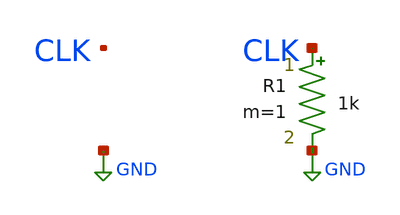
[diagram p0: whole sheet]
** sch_path: sim/jitter-calibration/testbench/tb_jitter_calibration.sch
**.subckt tb_jitter_calibration
R1 CLK GND 1k m=1
**** begin user architecture code

** GENERATED -- variant J10c: 300 cycles, nominal period
** 3.9170 ns, injected period jitter 1.000000% RMS
** (seeded RNG, seed 185010), TR = TF = 1 ns.
VCLK CLK GND pwl(  0.000000n 0 1.500000n 0 2.500000n 1.8 3.467587n 1.8  4.467587n 0 5.435174n 0
+ 6.435174n 1.8 7.412706n 1.8  8.412706n 0 9.390239n 0 10.390239n 1.8 11.309488n 1.8  12.309488n 0 13.228738n 0
+ 14.228738n 1.8 15.200628n 1.8  16.200628n 0 17.172519n 0 18.172519n 1.8 19.153921n 1.8  20.153921n 0
+ 21.135324n 0 22.135324n 1.8 23.078011n 1.8  24.078011n 0 25.020698n 0 26.020698n 1.8 26.951104n 1.8
+  27.951104n 0 28.881509n 0 29.881509n 1.8 30.850456n 1.8  31.850456n 0 32.819404n 0 33.819404n 1.8 34.771235n
+ 1.8  35.771235n 0 36.723066n 0 37.723066n 1.8 38.689098n 1.8  39.689098n 0 40.655130n 0 41.655130n 1.8
+ 42.608410n 1.8  43.608410n 0 44.561691n 0 45.561691n 1.8 46.506346n 1.8  47.506346n 0 48.451000n 0 49.451000n
+ 1.8 50.422296n 1.8  51.422296n 0 52.393592n 0 53.393592n 1.8 54.347858n 1.8  55.347858n 0 56.302123n 0
+ 57.302123n 1.8 58.256420n 1.8  59.256420n 0 60.210717n 0 61.210717n 1.8 62.173219n 1.8  63.173219n 0
+ 64.135720n 0 65.135720n 1.8 66.089666n 1.8  67.089666n 0 68.043611n 0 69.043611n 1.8 70.009970n 1.8
+  71.009970n 0 71.976329n 0 72.976329n 1.8 73.930021n 1.8  74.930021n 0 75.883714n 0 76.883714n 1.8 77.869536n
+ 1.8  78.869536n 0 79.855357n 0 80.855357n 1.8 81.766974n 1.8  82.766974n 0 83.678592n 0 84.678592n 1.8
+ 85.653946n 1.8  86.653946n 0 87.629300n 0 88.629300n 1.8 89.565099n 1.8  90.565099n 0 91.500898n 0 92.500898n
+ 1.8 93.444309n 1.8  94.444309n 0 95.387720n 0 96.387720n 1.8 97.308553n 1.8  98.308553n 0 99.229386n 0
+ 100.229386n 1.8 101.204522n 1.8  102.204522n 0 103.179659n 0 104.179659n 1.8 105.107584n 1.8  106.107584n 0
+ 107.035510n 0 108.035510n 1.8 108.976588n 1.8  109.976588n 0 110.917665n 0 111.917665n 1.8 112.867539n 1.8
+  113.867539n 0 114.817412n 0 115.817412n 1.8 116.788125n 1.8  117.788125n 0 118.758838n 0 119.758838n 1.8
+ 120.705444n 1.8  121.705444n 0 122.652051n 0 123.652051n 1.8 124.610528n 1.8  125.610528n 0 126.569005n 0
+ 127.569005n 1.8 128.502948n 1.8  129.502948n 0 130.436891n 0 131.436891n 1.8 132.374925n 1.8  133.374925n 0
+ 134.312958n 0 135.312958n 1.8 136.284613n 1.8  137.284613n 0 138.256268n 0 139.256268n 1.8 140.186354n 1.8
+  141.186354n 0 142.116440n 0 143.116440n 1.8 144.083552n 1.8  145.083552n 0 146.050664n 0 147.050664n 1.8
+ 148.011420n 1.8  149.011420n 0 149.972176n 0 150.972176n 1.8 151.931191n 1.8  152.931191n 0 153.890206n 0
+ 154.890206n 1.8 155.821172n 1.8  156.821172n 0 157.752138n 0 158.752138n 1.8 159.703538n 1.8  160.703538n 0
+ 161.654938n 0 162.654938n 1.8 163.603802n 1.8  164.603802n 0 165.552666n 0 166.552666n 1.8 167.494949n 1.8
+  168.494949n 0 169.437233n 0 170.437233n 1.8 171.428640n 1.8  172.428640n 0 173.420048n 0 174.420048n 1.8
+ 175.354551n 1.8  176.354551n 0 177.289054n 0 178.289054n 1.8 179.229152n 1.8  180.229152n 0 181.169250n 0
+ 182.169250n 1.8 183.108568n 1.8  184.108568n 0 185.047886n 0 186.047886n 1.8 186.977655n 1.8  187.977655n 0
+ 188.907423n 0 189.907423n 1.8 190.855155n 1.8  191.855155n 0 192.802888n 0 193.802888n 1.8 194.758147n 1.8
+  195.758147n 0 196.713406n 0 197.713406n 1.8 198.647563n 1.8  199.647563n 0 200.581720n 0 201.581720n 1.8
+ 202.490503n 1.8  203.490503n 0 204.399286n 0 205.399286n 1.8 206.354163n 1.8  207.354163n 0 208.309039n 0
+ 209.309039n 1.8 210.263509n 1.8  211.263509n 0 212.217979n 0 213.217979n 1.8 214.190097n 1.8  215.190097n 0
+ 216.162214n 0 217.162214n 1.8 218.112178n 1.8  219.112178n 0 220.062141n 0 221.062141n 1.8 222.028435n 1.8
+  223.028435n 0 223.994728n 0 224.994728n 1.8 225.974648n 1.8  226.974648n 0 227.954567n 0 228.954567n 1.8
+ 229.901638n 1.8  230.901638n 0 231.848708n 0 232.848708n 1.8 233.815738n 1.8  234.815738n 0 235.782768n 0
+ 236.782768n 1.8 237.752998n 1.8  238.752998n 0 239.723229n 0 240.723229n 1.8 241.679197n 1.8  242.679197n 0
+ 243.635165n 0 244.635165n 1.8 245.579002n 1.8  246.579002n 0 247.522838n 0 248.522838n 1.8 249.470750n 1.8
+  250.470750n 0 251.418663n 0 252.418663n 1.8 253.424114n 1.8  254.424114n 0 255.429565n 0 256.429565n 1.8
+ 257.421423n 1.8  258.421423n 0 259.413281n 0 260.413281n 1.8 261.371691n 1.8  262.371691n 0 263.330100n 0
+ 264.330100n 1.8 265.331600n 1.8  266.331600n 0 267.333100n 0 268.333100n 1.8 269.275644n 1.8  270.275644n 0
+ 271.218188n 0 272.218188n 1.8 273.182219n 1.8  274.182219n 0 275.146251n 0 276.146251n 1.8 277.122987n 1.8
+  278.122987n 0 279.099724n 0 280.099724n 1.8 281.059622n 1.8  282.059622n 0 283.019520n 0 284.019520n 1.8
+ 284.976046n 1.8  285.976046n 0 286.932571n 0 287.932571n 1.8 288.866826n 1.8  289.866826n 0 290.801080n 0
+ 291.801080n 1.8 292.718970n 1.8  293.718970n 0 294.636859n 0 295.636859n 1.8 296.602262n 1.8  297.602262n 0
+ 298.567664n 0 299.567664n 1.8 300.514107n 1.8  301.514107n 0 302.460550n 0 303.460550n 1.8 304.452856n 1.8
+  305.452856n 0 306.445163n 0 307.445163n 1.8 308.358824n 1.8  309.358824n 0 310.272485n 0 311.272485n 1.8
+ 312.204532n 1.8  313.204532n 0 314.136578n 0 315.136578n 1.8 316.094694n 1.8  317.094694n 0 318.052810n 0
+ 319.052810n 1.8 320.001457n 1.8  321.001457n 0 321.950104n 0 322.950104n 1.8 323.893454n 1.8  324.893454n 0
+ 325.836804n 0 326.836804n 1.8 327.820440n 1.8  328.820440n 0 329.804075n 0 330.804075n 1.8 331.750001n 1.8
+  332.750001n 0 333.695927n 0 334.695927n 1.8 335.657631n 1.8  336.657631n 0 337.619335n 0 338.619335n 1.8
+ 339.604657n 1.8  340.604657n 0 341.589979n 0 342.589979n 1.8 343.534561n 1.8  344.534561n 0 345.479143n 0
+ 346.479143n 1.8 347.428678n 1.8  348.428678n 0 349.378213n 0 350.378213n 1.8 351.316855n 1.8  352.316855n 0
+ 353.255497n 0 354.255497n 1.8 355.209135n 1.8  356.209135n 0 357.162773n 0 358.162773n 1.8 359.154792n 1.8
+  360.154792n 0 361.146811n 0 362.146811n 1.8 363.099707n 1.8  364.099707n 0 365.052604n 0 366.052604n 1.8
+ 367.000733n 1.8  368.000733n 0 368.948863n 0 369.948863n 1.8 370.905355n 1.8  371.905355n 0 372.861847n 0
+ 373.861847n 1.8 374.854057n 1.8  375.854057n 0 376.846266n 0 377.846266n 1.8 378.783298n 1.8  379.783298n 0
+ 380.720331n 0 381.720331n 1.8 382.691373n 1.8  383.691373n 0 384.662415n 0 385.662415n 1.8 386.617329n 1.8
+  387.617329n 0 388.572244n 0 389.572244n 1.8 390.541558n 1.8  391.541558n 0 392.510873n 0 393.510873n 1.8
+ 394.455352n 1.8  395.455352n 0 396.399832n 0 397.399832n 1.8 398.379878n 1.8  399.379878n 0 400.359924n 0
+ 401.359924n 1.8 402.346665n 1.8  403.346665n 0 404.333407n 0 405.333407n 1.8 406.269845n 1.8  407.269845n 0
+ 408.206282n 0 409.206282n 1.8 410.179704n 1.8  411.179704n 0 412.153125n 0 413.153125n 1.8 414.072846n 1.8
+  415.072846n 0 415.992567n 0 416.992567n 1.8 417.953025n 1.8  418.953025n 0 419.913483n 0 420.913483n 1.8
+ 421.859298n 1.8  422.859298n 0 423.805114n 0 424.805114n 1.8 425.734864n 1.8  426.734864n 0 427.664615n 0
+ 428.664615n 1.8 429.634682n 1.8  430.634682n 0 431.604749n 0 432.604749n 1.8 433.567902n 1.8  434.567902n 0
+ 435.531054n 0 436.531054n 1.8 437.506541n 1.8  438.506541n 0 439.482028n 0 440.482028n 1.8 441.430071n 1.8
+  442.430071n 0 443.378114n 0 444.378114n 1.8 445.341175n 1.8  446.341175n 0 447.304236n 0 448.304236n 1.8
+ 449.254138n 1.8  450.254138n 0 451.204040n 0 452.204040n 1.8 453.183686n 1.8  454.183686n 0 455.163332n 0
+ 456.163332n 1.8 457.105453n 1.8  458.105453n 0 459.047574n 0 460.047574n 1.8 460.997655n 1.8  461.997655n 0
+ 462.947736n 0 463.947736n 1.8 464.909671n 1.8  465.909671n 0 466.871606n 0 467.871606n 1.8 468.820058n 1.8
+  469.820058n 0 470.768510n 0 471.768510n 1.8 472.716913n 1.8  473.716913n 0 474.665317n 0 475.665317n 1.8
+ 476.629255n 1.8  477.629255n 0 478.593193n 0 479.593193n 1.8 480.569885n 1.8  481.569885n 0 482.546576n 0
+ 483.546576n 1.8 484.509378n 1.8  485.509378n 0 486.472179n 0 487.472179n 1.8 488.435751n 1.8  489.435751n 0
+ 490.399322n 0 491.399322n 1.8 492.356471n 1.8  493.356471n 0 494.313621n 0 495.313621n 1.8 496.311841n 1.8
+  497.311841n 0 498.310062n 0 499.310062n 1.8 500.281417n 1.8  501.281417n 0 502.252772n 0 503.252772n 1.8
+ 504.223085n 1.8  505.223085n 0 506.193398n 0 507.193398n 1.8 508.172969n 1.8  509.172969n 0 510.152540n 0
+ 511.152540n 1.8 512.150574n 1.8  513.150574n 0 514.148607n 0 515.148607n 1.8 516.108316n 1.8  517.108316n 0
+ 518.068024n 0 519.068024n 1.8 520.021929n 1.8  521.021929n 0 521.975834n 0 522.975834n 1.8 523.956108n 1.8
+  524.956108n 0 525.936381n 0 526.936381n 1.8 527.903064n 1.8  528.903064n 0 529.869747n 0 530.869747n 1.8
+ 531.853980n 1.8  532.853980n 0 533.838214n 0 534.838214n 1.8 535.816551n 1.8  536.816551n 0 537.794889n 0
+ 538.794889n 1.8 539.727189n 1.8  540.727189n 0 541.659489n 0 542.659489n 1.8 543.641375n 1.8  544.641375n 0
+ 545.623261n 0 546.623261n 1.8 547.605233n 1.8  548.605233n 0 549.587204n 0 550.587204n 1.8 551.560022n 1.8
+  552.560022n 0 553.532839n 0 554.532839n 1.8 555.485706n 1.8  556.485706n 0 557.438573n 0 558.438573n 1.8
+ 559.410459n 1.8  560.410459n 0 561.382345n 0 562.382345n 1.8 563.355811n 1.8  564.355811n 0 565.329276n 0
+ 566.329276n 1.8 567.285830n 1.8  568.285830n 0 569.242384n 0 570.242384n 1.8 571.212968n 1.8  572.212968n 0
+ 573.183552n 0 574.183552n 1.8 575.168164n 1.8  576.168164n 0 577.152777n 0 578.152777n 1.8 579.150439n 1.8
+  580.150439n 0 581.148101n 0 582.148101n 1.8 583.071739n 1.8  584.071739n 0 584.995377n 0 585.995377n 1.8
+ 586.939910n 1.8  587.939910n 0 588.884444n 0 589.884444n 1.8 590.831208n 1.8  591.831208n 0 592.777972n 0
+ 593.777972n 1.8 594.738809n 1.8  595.738809n 0 596.699645n 0 597.699645n 1.8 598.654166n 1.8  599.654166n 0
+ 600.608686n 0 601.608686n 1.8 602.593648n 1.8  603.593648n 0 604.578610n 0 605.578610n 1.8 606.545995n 1.8
+  607.545995n 0 608.513380n 0 609.513380n 1.8 610.456717n 1.8  611.456717n 0 612.400053n 0 613.400053n 1.8
+ 614.369379n 1.8  615.369379n 0 616.338706n 0 617.338706n 1.8 618.322239n 1.8  619.322239n 0 620.305773n 0
+ 621.305773n 1.8 622.258676n 1.8  623.258676n 0 624.211580n 0 625.211580n 1.8 626.163616n 1.8  627.163616n 0
+ 628.115652n 0 629.115652n 1.8 630.110946n 1.8  631.110946n 0 632.106239n 0 633.106239n 1.8 634.094996n 1.8
+  635.094996n 0 636.083753n 0 637.083753n 1.8 638.022007n 1.8  639.022007n 0 639.960262n 0 640.960262n 1.8
+ 641.944529n 1.8  642.944529n 0 643.928795n 0 644.928795n 1.8 645.874505n 1.8  646.874505n 0 647.820216n 0
+ 648.820216n 1.8 649.801482n 1.8  650.801482n 0 651.782748n 0 652.782748n 1.8 653.747596n 1.8  654.747596n 0
+ 655.712444n 0 656.712444n 1.8 657.678982n 1.8  658.678982n 0 659.645520n 0 660.645520n 1.8 661.591855n 1.8
+  662.591855n 0 663.538191n 0 664.538191n 1.8 665.485187n 1.8  666.485187n 0 667.432183n 0 668.432183n 1.8
+ 669.419227n 1.8  670.419227n 0 671.406271n 0 672.406271n 1.8 673.327805n 1.8  674.327805n 0 675.249339n 0
+ 676.249339n 1.8 677.232033n 1.8  678.232033n 0 679.214728n 0 680.214728n 1.8 681.164308n 1.8  682.164308n 0
+ 683.113889n 0 684.113889n 1.8 685.070725n 1.8  686.070725n 0 687.027561n 0 688.027561n 1.8 688.951112n 1.8
+  689.951112n 0 690.874662n 0 691.874662n 1.8 692.824420n 1.8  693.824420n 0 694.774178n 0 695.774178n 1.8
+ 696.726560n 1.8  697.726560n 0 698.678943n 0 699.678943n 1.8 700.652020n 1.8  701.652020n 0 702.625096n 0
+ 703.625096n 1.8 704.580270n 1.8  705.580270n 0 706.535444n 0 707.535444n 1.8 708.505501n 1.8  709.505501n 0
+ 710.475557n 0 711.475557n 1.8 712.421978n 1.8  713.421978n 0 714.368399n 0 715.368399n 1.8 716.348113n 1.8
+  717.348113n 0 718.327828n 0 719.327828n 1.8 720.286338n 1.8  721.286338n 0 722.244848n 0 723.244848n 1.8
+ 724.212968n 1.8  725.212968n 0 726.181087n 0 727.181087n 1.8 728.160394n 1.8  729.160394n 0 730.139702n 0
+ 731.139702n 1.8 732.088990n 1.8  733.088990n 0 734.038277n 0 735.038277n 1.8 735.991439n 1.8  736.991439n 0
+ 737.944601n 0 738.944601n 1.8 739.904355n 1.8  740.904355n 0 741.864108n 0 742.864108n 1.8 743.838251n 1.8
+  744.838251n 0 745.812393n 0 746.812393n 1.8 747.749591n 1.8  748.749591n 0 749.686789n 0 750.686789n 1.8
+ 751.650370n 1.8  752.650370n 0 753.613950n 0 754.613950n 1.8 755.573553n 1.8  756.573553n 0 757.533156n 0
+ 758.533156n 1.8 759.486980n 1.8  760.486980n 0 761.440804n 0 762.440804n 1.8 763.414867n 1.8  764.414867n 0
+ 765.388930n 0 766.388930n 1.8 767.379078n 1.8  768.379078n 0 769.369225n 0 770.369225n 1.8 771.333516n 1.8
+  772.333516n 0 773.297807n 0 774.297807n 1.8 775.209412n 1.8  776.209412n 0 777.121017n 0 778.121017n 1.8
+ 779.089050n 1.8  780.089050n 0 781.057084n 0 782.057084n 1.8 783.036384n 1.8  784.036384n 0 785.015684n 0
+ 786.015684n 1.8 787.000672n 1.8  788.000672n 0 788.985660n 0 789.985660n 1.8 790.919575n 1.8  791.919575n 0
+ 792.853490n 0 793.853490n 1.8 794.821912n 1.8  795.821912n 0 796.790334n 0 797.790334n 1.8 798.738880n 1.8
+  799.738880n 0 800.687425n 0 801.687425n 1.8 802.663109n 1.8  803.663109n 0 804.638793n 0 805.638793n 1.8
+ 806.576830n 1.8  807.576830n 0 808.514868n 0 809.514868n 1.8 810.476025n 1.8  811.476025n 0 812.437183n 0
+ 813.437183n 1.8 814.387642n 1.8  815.387642n 0 816.338101n 0 817.338101n 1.8 818.257021n 1.8  819.257021n 0
+ 820.175940n 0 821.175940n 1.8 822.089536n 1.8  823.089536n 0 824.003131n 0 825.003131n 1.8 825.950594n 1.8
+  826.950594n 0 827.898057n 0 828.898057n 1.8 829.878284n 1.8  830.878284n 0 831.858510n 0 832.858510n 1.8
+ 833.817286n 1.8  834.817286n 0 835.776062n 0 836.776062n 1.8 837.753702n 1.8  838.753702n 0 839.731342n 0
+ 840.731342n 1.8 841.673754n 1.8  842.673754n 0 843.616167n 0 844.616167n 1.8 845.558898n 1.8  846.558898n 0
+ 847.501629n 0 848.501629n 1.8 849.460750n 1.8  850.460750n 0 851.419870n 0 852.419870n 1.8 853.366837n 1.8
+  854.366837n 0 855.313804n 0 856.313804n 1.8 857.300954n 1.8  858.300954n 0 859.288103n 0 860.288103n 1.8
+ 861.269714n 1.8  862.269714n 0 863.251325n 0 864.251325n 1.8 865.231208n 1.8  866.231208n 0 867.211090n 0
+ 868.211090n 1.8 869.145106n 1.8  870.145106n 0 871.079121n 0 872.079121n 1.8 873.066848n 1.8  874.066848n 0
+ 875.054574n 0 876.054574n 1.8 877.001563n 1.8  878.001563n 0 878.948552n 0 879.948552n 1.8 880.922436n 1.8
+  881.922436n 0 882.896320n 0 883.896320n 1.8 884.858595n 1.8  885.858595n 0 886.820870n 0 887.820870n 1.8
+ 888.795133n 1.8  889.795133n 0 890.769397n 0 891.769397n 1.8 892.728198n 1.8  893.728198n 0 894.686998n 0
+ 895.686998n 1.8 896.647773n 1.8  897.647773n 0 898.608547n 0 899.608547n 1.8 900.580286n 1.8  901.580286n 0
+ 902.552026n 0 903.552026n 1.8 904.486650n 1.8  905.486650n 0 906.421275n 0 907.421275n 1.8 908.356793n 1.8
+  909.356793n 0 910.292312n 0 911.292312n 1.8 912.252178n 1.8  913.252178n 0 914.212044n 0 915.212044n 1.8
+ 916.150742n 1.8  917.150742n 0 918.089440n 0 919.089440n 1.8 920.051699n 1.8  921.051699n 0 922.013959n 0
+ 923.013959n 1.8 923.948531n 1.8  924.948531n 0 925.883104n 0 926.883104n 1.8 927.856976n 1.8  928.856976n 0
+ 929.830847n 0 930.830847n 1.8 931.809521n 1.8  932.809521n 0 933.788194n 0 934.788194n 1.8 935.751786n 1.8
+  936.751786n 0 937.715378n 0 938.715378n 1.8 939.667710n 1.8  940.667710n 0 941.620043n 0 942.620043n 1.8
+ 943.583472n 1.8  944.583472n 0 945.546901n 0 946.546901n 1.8 947.494216n 1.8  948.494216n 0 949.441530n 0
+ 950.441530n 1.8 951.394758n 1.8  952.394758n 0 953.347985n 0 954.347985n 1.8 955.308677n 1.8  956.308677n 0
+ 957.269369n 0 958.269369n 1.8 959.218937n 1.8  960.218937n 0 961.168505n 0 962.168505n 1.8 963.121270n 1.8
+  964.121270n 0 965.074035n 0 966.074035n 1.8 967.037774n 1.8  968.037774n 0 969.001514n 0 970.001514n 1.8
+ 970.926237n 1.8  971.926237n 0 972.850960n 0 973.850960n 1.8 974.778496n 1.8  975.778496n 0 976.706032n 0
+ 977.706032n 1.8 978.675056n 1.8  979.675056n 0 980.644081n 0 981.644081n 1.8 982.587678n 1.8  983.587678n 0
+ 984.531275n 0 985.531275n 1.8 986.489825n 1.8  987.489825n 0 988.448376n 0 989.448376n 1.8 990.392004n 1.8
+  991.392004n 0 992.335633n 0 993.335633n 1.8 994.293223n 1.8  995.293223n 0 996.250814n 0 997.250814n 1.8
+ 998.197855n 1.8  999.197855n 0 1000.144896n 0 1001.144896n 1.8 1002.105288n 1.8  1003.105288n 0 1004.065680n 0
+ 1005.065680n 1.8 1006.035468n 1.8  1007.035468n 0 1008.005256n 0 1009.005256n 1.8 1009.948835n 1.8  1010.948835n
+ 0 1011.892414n 0 1012.892414n 1.8 1013.836265n 1.8  1014.836265n 0 1015.780116n 0 1016.780116n 1.8
+ 1017.714073n 1.8  1018.714073n 0 1019.648030n 0 1020.648030n 1.8 1021.641457n 1.8  1022.641457n 0 1023.634885n 0
+ 1024.634885n 1.8 1025.642013n 1.8  1026.642013n 0 1027.649140n 0 1028.649140n 1.8 1029.578496n 1.8  1030.578496n
+ 0 1031.507852n 0 1032.507852n 1.8 1033.477170n 1.8  1034.477170n 0 1035.446489n 0 1036.446489n 1.8
+ 1037.468203n 1.8  1038.468203n 0 1039.489918n 0 1040.489918n 1.8 1041.431841n 1.8  1042.431841n 0 1043.373765n 0
+ 1044.373765n 1.8 1045.340315n 1.8  1046.340315n 0 1047.306866n 0 1048.306866n 1.8 1049.287459n 1.8  1050.287459n
+ 0 1051.268051n 0 1052.268051n 1.8 1053.246873n 1.8  1054.246873n 0 1055.225695n 0 1056.225695n 1.8
+ 1057.200454n 1.8  1058.200454n 0 1059.175214n 0 1060.175214n 1.8 1061.129622n 1.8  1062.129622n 0 1063.084030n 0
+ 1064.084030n 1.8 1065.037482n 1.8  1066.037482n 0 1066.990935n 0 1067.990935n 1.8 1068.972420n 1.8  1069.972420n
+ 0 1070.953905n 0 1071.953905n 1.8 1072.873984n 1.8  1073.873984n 0 1074.794062n 0 1075.794062n 1.8
+ 1076.739220n 1.8  1077.739220n 0 1078.684379n 0 1079.684379n 1.8 1080.638503n 1.8  1081.638503n 0 1082.592627n 0
+ 1083.592627n 1.8 1084.544284n 1.8  1085.544284n 0 1086.495940n 0 1087.495940n 1.8 1088.447910n 1.8  1089.447910n
+ 0 1090.399879n 0 1091.399879n 1.8 1092.344781n 1.8  1093.344781n 0 1094.289682n 0 1095.289682n 1.8
+ 1096.246190n 1.8  1097.246190n 0 1098.202697n 0 1099.202697n 1.8 1100.166301n 1.8  1101.166301n 0 1102.129905n 0
+ 1103.129905n 1.8 1104.053432n 1.8  1105.053432n 0 1105.976960n 0 1106.976960n 1.8 1107.927004n 1.8  1108.927004n
+ 0 1109.877048n 0 1110.877048n 1.8 1111.842071n 1.8  1112.842071n 0 1113.807094n 0 1114.807094n 1.8
+ 1115.781574n 1.8  1116.781574n 0 1117.756053n 0 1118.756053n 1.8 1119.749973n 1.8  1120.749973n 0 1121.743893n 0
+ 1122.743893n 1.8 1123.722007n 1.8  1124.722007n 0 1125.700122n 0 1126.700122n 1.8 1127.663556n 1.8  1128.663556n
+ 0 1129.626990n 0 1130.626990n 1.8 1131.582988n 1.8  1132.582988n 0 1133.538987n 0 1134.538987n 1.8
+ 1135.509294n 1.8  1136.509294n 0 1137.479601n 0 1138.479601n 1.8 1139.436287n 1.8  1140.436287n 0 1141.392973n 0
+ 1142.392973n 1.8 1143.373249n 1.8  1144.373249n 0 1145.353526n 0 1146.353526n 1.8 1147.350433n 1.8  1148.350433n
+ 0 1149.347341n 0 1150.347341n 1.8 1151.304029n 1.8  1152.304029n 0 1153.260718n 0 1154.260718n 1.8
+ 1155.200450n 1.8  1156.200450n 0 1157.140182n 0 1158.140182n 1.8 1159.063682n 1.8  1160.063682n 0 1160.987182n 0
+ 1161.987182n 1.8 1162.928879n 1.8  1163.928879n 0 1164.870576n 0 1165.870576n 1.8 1166.843522n 1.8  1167.843522n
+ 0 1168.816467n 0 1169.816467n 1.8 1170.753927n 1.8  1171.753927n 0 1172.691387n 0 1173.691387n 1.8
+ 1174.645694n 1.8  1175.645694n 0 1176.600000n 0 1177.600000n 1.8 1178.558500n 1.8  1179.558500n 0  )


** sky130 PDK model include (tt corner) -- patched per-point by sim/harness.
** No device in this testbench uses it: it is here so the harness's own
** corner substitution and this record's environment provenance are the same
** as every other campaign's. See this file's header comment.
.lib $::SKYWATER_MODELS/sky130.lib.spice tt
** No .tran/.print card here on purpose -- sim/harness/measure.py injects the
** analysis from this manifest's own measure block.

**** end user architecture code
**.ends
.GLOBAL GND
.end
